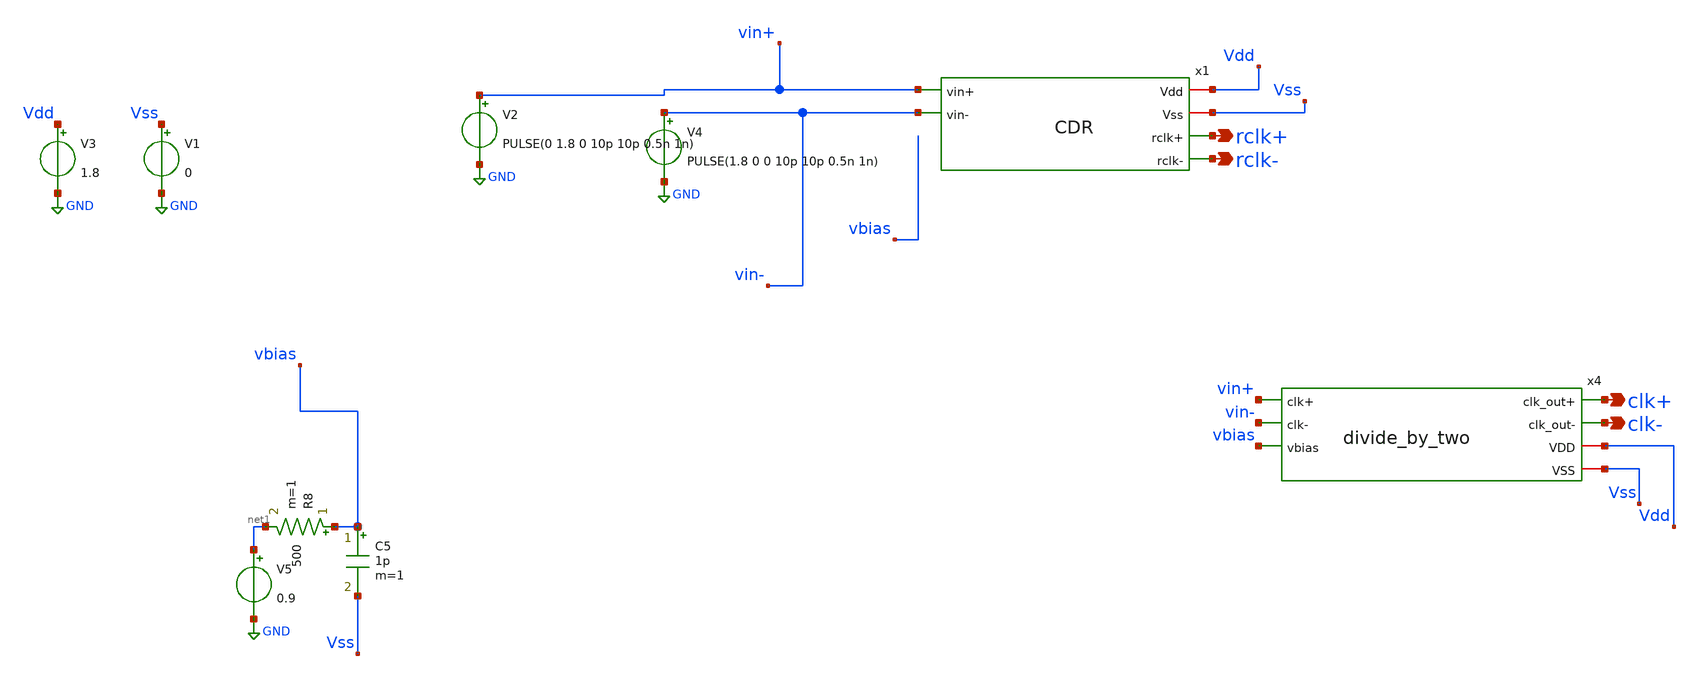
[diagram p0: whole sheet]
** sch_path: xschem/attic/demux_tb.sch
**.subckt demux_tb rclk- rclk+ clk- clk+
*.opin rclk-
*.opin rclk+
*.opin clk-
*.opin clk+
V3 Vdd GND 1.8
V1 Vss GND 0
V2 vin+ GND PULSE(0 1.8 0 10p 10p 0.5n 1n)
V4 vin- GND PULSE(1.8 0 0 10p 10p 0.5n 1n)
V5 net1 GND 0.9
R8 vbias net1 500 m=1
C5 vbias Vss 1p m=1
x1 Vdd vin+ Vss vin- rclk+ rclk- CDR
x4 clk+ clk- vin+ vin- vbias Vdd Vss divide_by_two
**** begin user architecture code



.lib /home/ttuser/pdk/sky130A/libs.tech/ngspice/sky130.lib.spice tt
.include /home/ttuser/pdk/sky130A/libs.ref/sky130_fd_sc_hd/spice/sky130_fd_sc_hd.spice
.options method=gear reltol=0.001 abstol=1e-12
.op
.control
  tran 10p 20n
  write demux_tb.raw
.endc



**** end user architecture code
**.ends
.GLOBAL GND
.end
